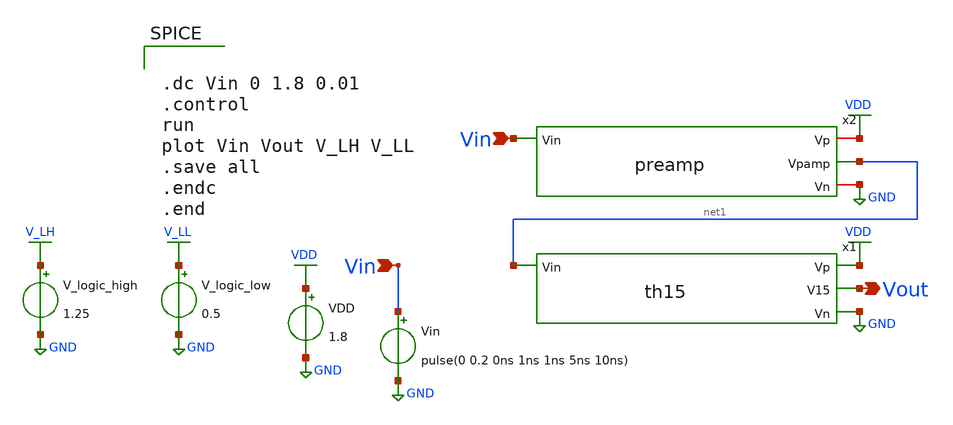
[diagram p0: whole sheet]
** sch_path: xschem/Vth_sch/Pre_layout/th15.sch
**.subckt th15 Vin Vout Vin
*.ipin Vin
*.opin Vout
*.ipin Vin
VDD VDD GND 1.8
Vin Vin GND pulse(0 0.2 0ns 1ns 1ns 5ns 10ns)
V_logic_high V_LH GND 1.25
V_logic_low V_LL GND 0.5
x1 VDD Vout net1 GND th15
x2 VDD Vin net1 GND preamp
**** begin user architecture code


.lib /usr/local/share/pdk/sky130A/libs.tech/ngspice/sky130.lib.spice tt

.save all





.dc Vin 0 1.8 0.01
.control
run
plot Vin Vout V_LH V_LL
.save all
.endc
.end


**** end user architecture code
**.ends

* expanding   symbol:  /home/exotic/Desktop/ASIC_ADC/xschem/Vth_sch/Symbol/th15.sym # of pins=4
** sym_path: xschem/Vth_sch/Symbol/th15.sym
** sch_path: xschem/Vth_sch/Symbol/th15.sch
.subckt th15 Vp V15 Vin Vn
*.opin Vn
*.opin Vp
*.ipin Vin
*.opin V15
XM3 V15 net1 Vp Vp sky130_fd_pr__pfet_01v8 L=3.3 W=0.421 nf=1 ad='int((nf+1)/2) * W/nf * 0.29' as='int((nf+2)/2) * W/nf * 0.29'
+ pd='2*int((nf+1)/2) * (W/nf + 0.29)' ps='2*int((nf+2)/2) * (W/nf + 0.29)' nrd='0.29 / W' nrs='0.29 / W'
+ sa=0 sb=0 sd=0 mult=1 m=1
XM4 V15 net1 Vn Vn sky130_fd_pr__nfet_01v8 L=0.15 W=2.51 nf=1 ad='int((nf+1)/2) * W/nf * 0.29' as='int((nf+2)/2) * W/nf * 0.29'
+ pd='2*int((nf+1)/2) * (W/nf + 0.29)' ps='2*int((nf+2)/2) * (W/nf + 0.29)' nrd='0.29 / W' nrs='0.29 / W'
+ sa=0 sb=0 sd=0 mult=1 m=1
XM2 net1 Vin Vp Vp sky130_fd_pr__pfet_01v8 L=0.79 W=0.51 nf=1 ad='int((nf+1)/2) * W/nf * 0.29' as='int((nf+2)/2) * W/nf * 0.29'
+ pd='2*int((nf+1)/2) * (W/nf + 0.29)' ps='2*int((nf+2)/2) * (W/nf + 0.29)' nrd='0.29 / W' nrs='0.29 / W'
+ sa=0 sb=0 sd=0 mult=1 m=1
XM1 net1 Vin net2 Vn sky130_fd_pr__nfet_01v8 L=2.0 W=0.36 nf=1 ad='int((nf+1)/2) * W/nf * 0.29' as='int((nf+2)/2) * W/nf * 0.29'
+ pd='2*int((nf+1)/2) * (W/nf + 0.29)' ps='2*int((nf+2)/2) * (W/nf + 0.29)' nrd='0.29 / W' nrs='0.29 / W'
+ sa=0 sb=0 sd=0 mult=1 m=1
XM0 Vn Vn net2 Vp sky130_fd_pr__pfet_01v8 L=0.285 W=0.5 nf=1 ad='int((nf+1)/2) * W/nf * 0.29' as='int((nf+2)/2) * W/nf * 0.29'
+ pd='2*int((nf+1)/2) * (W/nf + 0.29)' ps='2*int((nf+2)/2) * (W/nf + 0.29)' nrd='0.29 / W' nrs='0.29 / W'
+ sa=0 sb=0 sd=0 mult=1 m=1
.ends


* expanding   symbol:  /home/exotic/Desktop/ASIC_ADC/xschem/Vth_sch/Symbol/preamp.sym # of pins=4
** sym_path: xschem/Vth_sch/Symbol/preamp.sym
** sch_path: xschem/Vth_sch/Symbol/preamp.sch
.subckt preamp Vp Vin Vpamp Vn
*.ipin Vin
*.opin Vpamp
*.iopin Vp
*.iopin Vn
XM1 Vp Vin Vpamp Vn sky130_fd_pr__nfet_01v8 L=3.5 W=1 nf=1 ad='int((nf+1)/2) * W/nf * 0.29' as='int((nf+2)/2) * W/nf * 0.29'
+ pd='2*int((nf+1)/2) * (W/nf + 0.29)' ps='2*int((nf+2)/2) * (W/nf + 0.29)' nrd='0.29 / W' nrs='0.29 / W'
+ sa=0 sb=0 sd=0 mult=1 m=1
XM0 Vn Vin Vpamp Vp sky130_fd_pr__pfet_01v8 L=0.150 W=0.63 nf=1 ad='int((nf+1)/2) * W/nf * 0.29' as='int((nf+2)/2) * W/nf * 0.29'
+ pd='2*int((nf+1)/2) * (W/nf + 0.29)' ps='2*int((nf+2)/2) * (W/nf + 0.29)' nrd='0.29 / W' nrs='0.29 / W'
+ sa=0 sb=0 sd=0 mult=1 m=1
.ends

.GLOBAL VDD
.GLOBAL GND
.GLOBAL V_LH
.GLOBAL V_LL
.end
